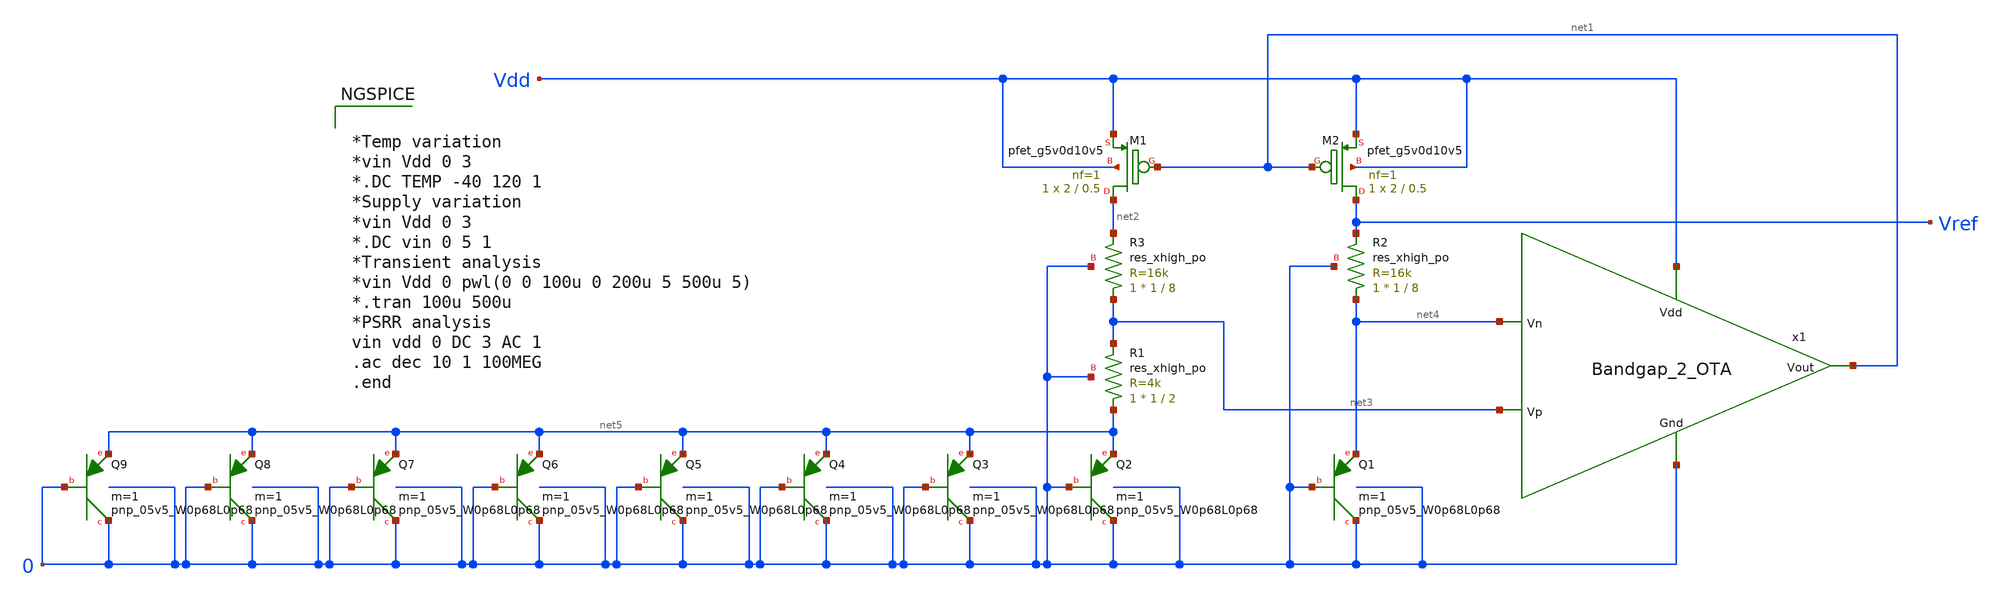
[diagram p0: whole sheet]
** sch_path: Bandgap/Schematics/BGR_2/Bandgap_2.sch
**.subckt Bandgap_2
XM1 net2 net1 Vdd Vdd sky130_fd_pr__pfet_g5v0d10v5 L=0.5 W=2 nf=1 ad='int((nf+1)/2) * W/nf * 0.29' as='int((nf+2)/2) * W/nf * 0.29'
+ pd='2*int((nf+1)/2) * (W/nf + 0.29)' ps='2*int((nf+2)/2) * (W/nf + 0.29)' nrd='0.29 / W' nrs='0.29 / W'
+ sa=0 sb=0 sd=0 mult=1 m=1
XM2 Vref net1 Vdd Vdd sky130_fd_pr__pfet_g5v0d10v5 L=0.5 W=2 nf=1 ad='int((nf+1)/2) * W/nf * 0.29' as='int((nf+2)/2) * W/nf * 0.29'
+ pd='2*int((nf+1)/2) * (W/nf + 0.29)' ps='2*int((nf+2)/2) * (W/nf + 0.29)' nrd='0.29 / W' nrs='0.29 / W'
+ sa=0 sb=0 sd=0 mult=1 m=1
XR1 net5 net3 0 sky130_fd_pr__res_xhigh_po W=1 L=2 mult=1 m=1
XR2 net4 Vref 0 sky130_fd_pr__res_xhigh_po W=1 L=8 mult=1 m=1
XR3 net3 net2 0 sky130_fd_pr__res_xhigh_po W=1 L=8 mult=1 m=1
XQ1 0 0 net4 sky130_fd_pr__pnp_05v5_W0p68L0p68 m=1
XQ2 0 0 net5 sky130_fd_pr__pnp_05v5_W0p68L0p68 m=1
XQ3 0 0 net5 sky130_fd_pr__pnp_05v5_W0p68L0p68 m=1
XQ4 0 0 net5 sky130_fd_pr__pnp_05v5_W0p68L0p68 m=1
XQ5 0 0 net5 sky130_fd_pr__pnp_05v5_W0p68L0p68 m=1
XQ6 0 0 net5 sky130_fd_pr__pnp_05v5_W0p68L0p68 m=1
XQ7 0 0 net5 sky130_fd_pr__pnp_05v5_W0p68L0p68 m=1
XQ8 0 0 net5 sky130_fd_pr__pnp_05v5_W0p68L0p68 m=1
XQ9 0 0 net5 sky130_fd_pr__pnp_05v5_W0p68L0p68 m=1
x1 Vdd net1 net4 net3 0 Bandgap_2_OTA
**** begin user architecture code


*Temp variation
*vin Vdd 0 3
*.DC TEMP -40 120 1
*Supply variation
*vin Vdd 0 3
*.DC vin 0 5 1
*Transient analysis
*vin Vdd 0 pwl(0 0 100u 0 200u 5 500u 5)
*.tran 100u 500u
*PSRR analysis
vin vdd 0 DC 3 AC 1
.ac dec 10 1 100MEG
.end



.include $::SKYWATER_MODELS/cells/nfet_01v8/sky130_fd_pr__nfet_01v8__tt.corner.spice
.include $::SKYWATER_MODELS/cells/nfet_01v8_lvt/sky130_fd_pr__nfet_01v8_lvt__tt.corner.spice
.include $::SKYWATER_MODELS/cells/pfet_01v8/sky130_fd_pr__pfet_01v8__tt.corner.spice
.include $::SKYWATER_MODELS/cells/nfet_03v3_nvt/sky130_fd_pr__nfet_03v3_nvt__tt.corner.spice
.include $::SKYWATER_MODELS/cells/nfet_05v0_nvt/sky130_fd_pr__nfet_05v0_nvt__tt.corner.spice
.include $::SKYWATER_MODELS/cells/esd_nfet_01v8/sky130_fd_pr__esd_nfet_01v8__tt.corner.spice
.include $::SKYWATER_MODELS/cells/pfet_01v8_lvt/sky130_fd_pr__pfet_01v8_lvt__tt.corner.spice
.include $::SKYWATER_MODELS/cells/pfet_01v8_hvt/sky130_fd_pr__pfet_01v8_hvt__tt.corner.spice
.include $::SKYWATER_MODELS/cells/esd_pfet_g5v0d10v5/sky130_fd_pr__esd_pfet_g5v0d10v5__tt.corner.spice
.include $::SKYWATER_MODELS/cells/pfet_g5v0d10v5/sky130_fd_pr__pfet_g5v0d10v5__tt.corner.spice
.include $::SKYWATER_MODELS/cells/pfet_g5v0d16v0/sky130_fd_pr__pfet_g5v0d16v0__tt.corner.spice
.include $::SKYWATER_MODELS/cells/nfet_g5v0d10v5/sky130_fd_pr__nfet_g5v0d10v5__tt.corner.spice
.include $::SKYWATER_MODELS/cells/nfet_g5v0d16v0/sky130_fd_pr__nfet_g5v0d16v0__tt_discrete.corner.spice
.include $::SKYWATER_MODELS/cells/esd_nfet_g5v0d10v5/sky130_fd_pr__esd_nfet_g5v0d10v5__tt.corner.spice
.include $::SKYWATER_MODELS/models/corners/tt/nonfet.spice
* Mismatch parameters
.include $::SKYWATER_MODELS/cells/nfet_01v8/sky130_fd_pr__nfet_01v8__mismatch.corner.spice
.include $::SKYWATER_MODELS/cells/pfet_01v8/sky130_fd_pr__pfet_01v8__mismatch.corner.spice
.include $::SKYWATER_MODELS/cells/nfet_01v8_lvt/sky130_fd_pr__nfet_01v8_lvt__mismatch.corner.spice
.include $::SKYWATER_MODELS/cells/pfet_01v8_lvt/sky130_fd_pr__pfet_01v8_lvt__mismatch.corner.spice
.include $::SKYWATER_MODELS/cells/pfet_01v8_hvt/sky130_fd_pr__pfet_01v8_hvt__mismatch.corner.spice
.include $::SKYWATER_MODELS/cells/nfet_g5v0d10v5/sky130_fd_pr__nfet_g5v0d10v5__mismatch.corner.spice
.include $::SKYWATER_MODELS/cells/pfet_g5v0d10v5/sky130_fd_pr__pfet_g5v0d10v5__mismatch.corner.spice
.include $::SKYWATER_MODELS/cells/nfet_05v0_nvt/sky130_fd_pr__nfet_05v0_nvt__mismatch.corner.spice
.include $::SKYWATER_MODELS/cells/nfet_03v3_nvt/sky130_fd_pr__nfet_03v3_nvt__mismatch.corner.spice
* Resistor$::SKYWATER_MODELS/Capacitor
.include $::SKYWATER_MODELS/models/r+c/res_typical__cap_typical.spice
.include $::SKYWATER_MODELS/models/r+c/res_typical__cap_typical__lin.spice
* Special cells
.include $::SKYWATER_MODELS/models/corners/tt/specialized_cells.spice
* All models
.include $::SKYWATER_MODELS/models/all.spice
* Corner
.include $::SKYWATER_MODELS/models/corners/tt/rf.spice

**** end user architecture code
**.ends

* expanding   symbol:  /home/eslam/Analog_Design/Bandgap/Schematics/BGR_2/Bandgap_2_OTA.sym # of
*+ pins=5
** sym_path: Analog_Blocks/Bandgap/Schematics/BGR_2/Bandgap_2_OTA.sym
** sch_path: Analog_Blocks/Bandgap/Schematics/BGR_2/Bandgap_2_OTA.sch
.subckt Bandgap_2_OTA Vdd Vout Vn Vp Gnd
*.ipin Vdd
*.ipin Gnd
*.ipin Vn
*.ipin Vp
*.opin Vout
XM5 net3 net4 Vdd Vdd sky130_fd_pr__pfet_g5v0d10v5 L=1 W=10 nf=1 ad='int((nf+1)/2) * W/nf * 0.29' as='int((nf+2)/2) * W/nf * 0.29'
+ pd='2*int((nf+1)/2) * (W/nf + 0.29)' ps='2*int((nf+2)/2) * (W/nf + 0.29)' nrd='0.29 / W' nrs='0.29 / W'
+ sa=0 sb=0 sd=0 mult=1 m=1
XM7 Vout net4 Vdd Vdd sky130_fd_pr__pfet_g5v0d10v5 L=1 W=54 nf=1 ad='int((nf+1)/2) * W/nf * 0.29' as='int((nf+2)/2) * W/nf * 0.29'
+ pd='2*int((nf+1)/2) * (W/nf + 0.29)' ps='2*int((nf+2)/2) * (W/nf + 0.29)' nrd='0.29 / W' nrs='0.29 / W'
+ sa=0 sb=0 sd=0 mult=1 m=1
XM2 net1 Vp net3 Vdd sky130_fd_pr__pfet_g5v0d10v5 L=1 W=30 nf=1 ad='int((nf+1)/2) * W/nf * 0.29' as='int((nf+2)/2) * W/nf * 0.29'
+ pd='2*int((nf+1)/2) * (W/nf + 0.29)' ps='2*int((nf+2)/2) * (W/nf + 0.29)' nrd='0.29 / W' nrs='0.29 / W'
+ sa=0 sb=0 sd=0 mult=1 m=1
XM1 net2 Vn net3 Vdd sky130_fd_pr__pfet_g5v0d10v5 L=1 W=30 nf=1 ad='int((nf+1)/2) * W/nf * 0.29' as='int((nf+2)/2) * W/nf * 0.29'
+ pd='2*int((nf+1)/2) * (W/nf + 0.29)' ps='2*int((nf+2)/2) * (W/nf + 0.29)' nrd='0.29 / W' nrs='0.29 / W'
+ sa=0 sb=0 sd=0 mult=1 m=1
XM8 Vout net1 Gnd Gnd sky130_fd_pr__nfet_g5v0d10v5 L=0.5 W=75 nf=1 ad='int((nf+1)/2) * W/nf * 0.29' as='int((nf+2)/2) * W/nf * 0.29'
+ pd='2*int((nf+1)/2) * (W/nf + 0.29)' ps='2*int((nf+2)/2) * (W/nf + 0.29)' nrd='0.29 / W' nrs='0.29 / W'
+ sa=0 sb=0 sd=0 mult=1 m=1
XM4 net1 net2 Gnd Gnd sky130_fd_pr__nfet_g5v0d10v5 L=0.5 W=7.5 nf=1 ad='int((nf+1)/2) * W/nf * 0.29'
+ as='int((nf+2)/2) * W/nf * 0.29' pd='2*int((nf+1)/2) * (W/nf + 0.29)' ps='2*int((nf+2)/2) * (W/nf + 0.29)'
+ nrd='0.29 / W' nrs='0.29 / W' sa=0 sb=0 sd=0 mult=1 m=1
XM3 net2 net2 Gnd Gnd sky130_fd_pr__nfet_g5v0d10v5 L=0.5 W=7.5 nf=1 ad='int((nf+1)/2) * W/nf * 0.29'
+ as='int((nf+2)/2) * W/nf * 0.29' pd='2*int((nf+1)/2) * (W/nf + 0.29)' ps='2*int((nf+2)/2) * (W/nf + 0.29)'
+ nrd='0.29 / W' nrs='0.29 / W' sa=0 sb=0 sd=0 mult=1 m=1
XC1 net1 Vout sky130_fd_pr__cap_mim_m3_2 W=2 L=1 MF=1 m=1
XM6 net5 net4 Vdd Vdd sky130_fd_pr__pfet_g5v0d10v5 L=2 W=30 nf=1 ad='int((nf+1)/2) * W/nf * 0.29' as='int((nf+2)/2) * W/nf * 0.29'
+ pd='2*int((nf+1)/2) * (W/nf + 0.29)' ps='2*int((nf+2)/2) * (W/nf + 0.29)' nrd='0.29 / W' nrs='0.29 / W'
+ sa=0 sb=0 sd=0 mult=1 m=1
XM9 net4 net4 Vdd Vdd sky130_fd_pr__pfet_g5v0d10v5 L=2 W=30 nf=1 ad='int((nf+1)/2) * W/nf * 0.29' as='int((nf+2)/2) * W/nf * 0.29'
+ pd='2*int((nf+1)/2) * (W/nf + 0.29)' ps='2*int((nf+2)/2) * (W/nf + 0.29)' nrd='0.29 / W' nrs='0.29 / W'
+ sa=0 sb=0 sd=0 mult=1 m=1
XM10 net4 net5 net6 Gnd sky130_fd_pr__nfet_g5v0d10v5 L=5 W=15 nf=1 ad='int((nf+1)/2) * W/nf * 0.29' as='int((nf+2)/2) * W/nf * 0.29'
+ pd='2*int((nf+1)/2) * (W/nf + 0.29)' ps='2*int((nf+2)/2) * (W/nf + 0.29)' nrd='0.29 / W' nrs='0.29 / W'
+ sa=0 sb=0 sd=0 mult=1 m=1
XM11 net5 net5 Gnd Gnd sky130_fd_pr__nfet_g5v0d10v5 L=5 W=5 nf=1 ad='int((nf+1)/2) * W/nf * 0.29' as='int((nf+2)/2) * W/nf * 0.29'
+ pd='2*int((nf+1)/2) * (W/nf + 0.29)' ps='2*int((nf+2)/2) * (W/nf + 0.29)' nrd='0.29 / W' nrs='0.29 / W'
+ sa=0 sb=0 sd=0 mult=1 m=1
XR1 Gnd net6 Gnd sky130_fd_pr__res_xhigh_po W=1 L=3.7 mult=1 m=1
.ends

.end
